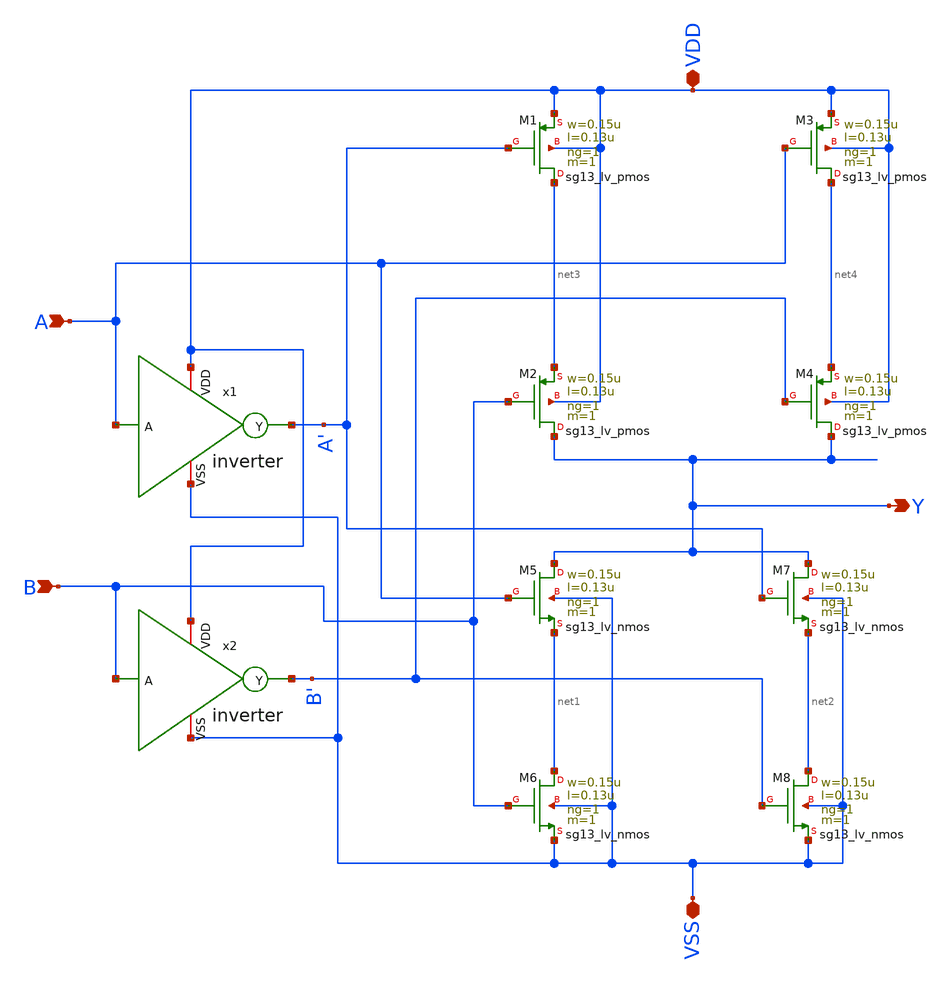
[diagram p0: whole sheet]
** sch_path: LogicGate/XOR2.sch
**.subckt XOR2 Y VSS VDD A B
*.opin Y
*.iopin VSS
*.iopin VDD
*.ipin A
*.ipin B
XM1 net3 A' VDD VDD sg13_lv_pmos w=0.15u l=0.13u ng=1 m=1 mm_ok=1
XM2 Y B net3 VDD sg13_lv_pmos w=0.15u l=0.13u ng=1 m=1 mm_ok=1
XM3 net4 A VDD VDD sg13_lv_pmos w=0.15u l=0.13u ng=1 m=1 mm_ok=1
XM4 Y B' net4 VDD sg13_lv_pmos w=0.15u l=0.13u ng=1 m=1 mm_ok=1
XM5 Y A net1 VSS sg13_lv_nmos w=0.15u l=0.13u ng=1 m=1 mm_ok=1
XM6 net1 B VSS VSS sg13_lv_nmos w=0.15u l=0.13u ng=1 m=1 mm_ok=1
XM7 Y A' net2 VSS sg13_lv_nmos w=0.15u l=0.13u ng=1 m=1 mm_ok=1
XM8 net2 B' VSS VSS sg13_lv_nmos w=0.15u l=0.13u ng=1 m=1 mm_ok=1
x1 VDD A A' VSS inverter
x2 VDD B B' VSS inverter
**.ends

* expanding   symbol:  /foss/designs/BTDay6-Ex/inverter.sym # of pins=4
** sym_path: BTDay6-Ex/inverter.sym
** sch_path: BTDay6-Ex/inverter.sch
.subckt inverter VDD A Y VSS
*.ipin A
*.opin Y
*.iopin VDD
*.iopin VSS
XM1 Y A VSS VSS sg13_lv_nmos w=0.15u l=0.13u ng=1 m=1 mm_ok=1
XM2 Y A VDD VDD sg13_lv_pmos w=0.15u l=0.13u ng=1 m=1 mm_ok=1
.ends

.end
